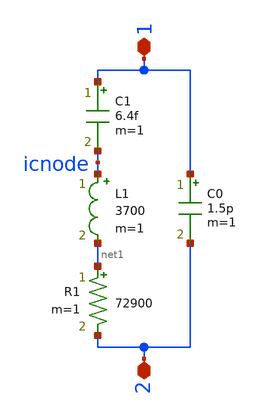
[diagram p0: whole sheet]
** sch_path: xschem/xtal_abs_040.sch
**.subckt xtal_abs_040 1 2
*.iopin 1
*.iopin 2
L1 icnode net1 3700 m=1
C1 1 icnode 6.4f m=1
C0 1 2 1.5p m=1
R1 net1 2 72900 m=1
**.ends
.end
